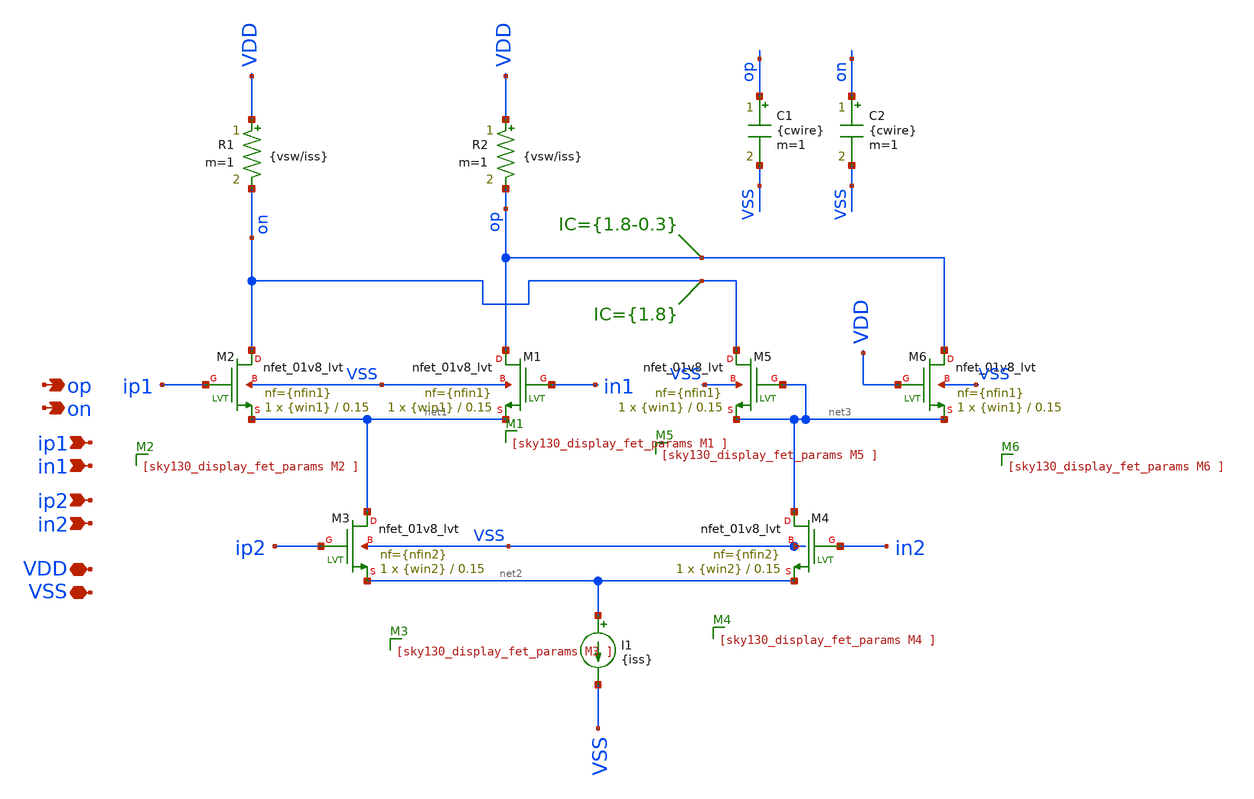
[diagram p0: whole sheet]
** sch_path: schematics/divider23/gate.sch
**.subckt gate VSS VDD op on ip1 in1 ip2 in2
*.iopin VSS
*.iopin VDD
*.opin op
*.opin on
*.ipin ip1
*.ipin in1
*.ipin ip2
*.ipin in2
XM2 on ip1 net1 VSS sky130_fd_pr__nfet_01v8_lvt L=0.15 W={win1} nf={nfin1} ad='int(({nfin1} + 1)/2) * {win1} / {nfin1} * 0.29'
+ as='int(({nfin1} + 2)/2) * {win1} / {nfin1} * 0.29' pd='2*int(({nfin1} + 1)/2) * ({win1} / {nfin1} + 0.29)'
+ ps='2*int(({nfin1} + 2)/2) * ({win1} / {nfin1} + 0.29)' nrd='0.29 / {win1} ' nrs='0.29 / {win1} ' sa=0
+ sb=0 sd=0 mult=1 m=1
XM1 op in1 net1 VSS sky130_fd_pr__nfet_01v8_lvt L=0.15 W={win1} nf={nfin1} ad='int(({nfin1} + 1)/2) * {win1} / {nfin1} * 0.29'
+ as='int(({nfin1} + 2)/2) * {win1} / {nfin1} * 0.29' pd='2*int(({nfin1} + 1)/2) * ({win1} / {nfin1} + 0.29)'
+ ps='2*int(({nfin1} + 2)/2) * ({win1} / {nfin1} + 0.29)' nrd='0.29 / {win1} ' nrs='0.29 / {win1} ' sa=0
+ sb=0 sd=0 mult=1 m=1
I1 net2 VSS {iss}
XM3 net1 ip2 net2 VSS sky130_fd_pr__nfet_01v8_lvt L=0.15 W={win2} nf={nfin2} ad='int(({nfin2} + 1)/2) * {win2} / {nfin2} * 0.29'
+ as='int(({nfin2} + 2)/2) * {win2} / {nfin2} * 0.29' pd='2*int(({nfin2} + 1)/2) * ({win2} / {nfin2} + 0.29)'
+ ps='2*int(({nfin2} + 2)/2) * ({win2} / {nfin2} + 0.29)' nrd='0.29 / {win2} ' nrs='0.29 / {win2} ' sa=0
+ sb=0 sd=0 mult=1 m=1
XM4 net3 in2 net2 VSS sky130_fd_pr__nfet_01v8_lvt L=0.15 W={win2} nf={nfin2} ad='int(({nfin2} + 1)/2) * {win2} / {nfin2} * 0.29'
+ as='int(({nfin2} + 2)/2) * {win2} / {nfin2} * 0.29' pd='2*int(({nfin2} + 1)/2) * ({win2} / {nfin2} + 0.29)'
+ ps='2*int(({nfin2} + 2)/2) * ({win2} / {nfin2} + 0.29)' nrd='0.29 / {win2} ' nrs='0.29 / {win2} ' sa=0
+ sb=0 sd=0 mult=1 m=1
XM5 on net3 net3 VSS sky130_fd_pr__nfet_01v8_lvt L=0.15 W={win1} nf={nfin1} ad='int(({nfin1} + 1)/2) * {win1} / {nfin1} * 0.29'
+ as='int(({nfin1} + 2)/2) * {win1} / {nfin1} * 0.29' pd='2*int(({nfin1} + 1)/2) * ({win1} / {nfin1} + 0.29)'
+ ps='2*int(({nfin1} + 2)/2) * ({win1} / {nfin1} + 0.29)' nrd='0.29 / {win1} ' nrs='0.29 / {win1} ' sa=0
+ sb=0 sd=0 mult=1 m=1
XM6 op VDD net3 VSS sky130_fd_pr__nfet_01v8_lvt L=0.15 W={win1} nf={nfin1} ad='int(({nfin1} + 1)/2) * {win1} / {nfin1} * 0.29'
+ as='int(({nfin1} + 2)/2) * {win1} / {nfin1} * 0.29' pd='2*int(({nfin1} + 1)/2) * ({win1} / {nfin1} + 0.29)'
+ ps='2*int(({nfin1} + 2)/2) * ({win1} / {nfin1} + 0.29)' nrd='0.29 / {win1} ' nrs='0.29 / {win1} ' sa=0
+ sb=0 sd=0 mult=1 m=1
C1 op VSS {cwire} m=1
C2 on VSS {cwire} m=1
.IC V(op)={1.8-0.3}
.IC V(on)={1.8}
R1 VDD on {vsw/iss} m=1
R2 VDD op {vsw/iss} m=1
**.ends
.end
